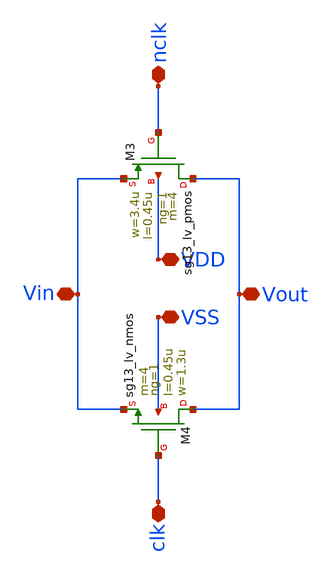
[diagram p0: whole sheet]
** sch_path: unic_cass_wrapper_user_project/ROs_reliability/tgate_force.sch
**.subckt tgate_force nclk clk VDD VSS Vout Vin
*.iopin nclk
*.iopin clk
*.iopin VDD
*.iopin VSS
*.iopin Vout
*.iopin Vin
XM3 Vout nclk Vin VDD sg13_lv_pmos w=3.4u l=0.45u ng=1 m=4 mm_ok=1
XM4 Vout clk Vin VSS sg13_lv_nmos w=1.3u l=0.45u ng=1 m=4 mm_ok=1
**.ends
.end
